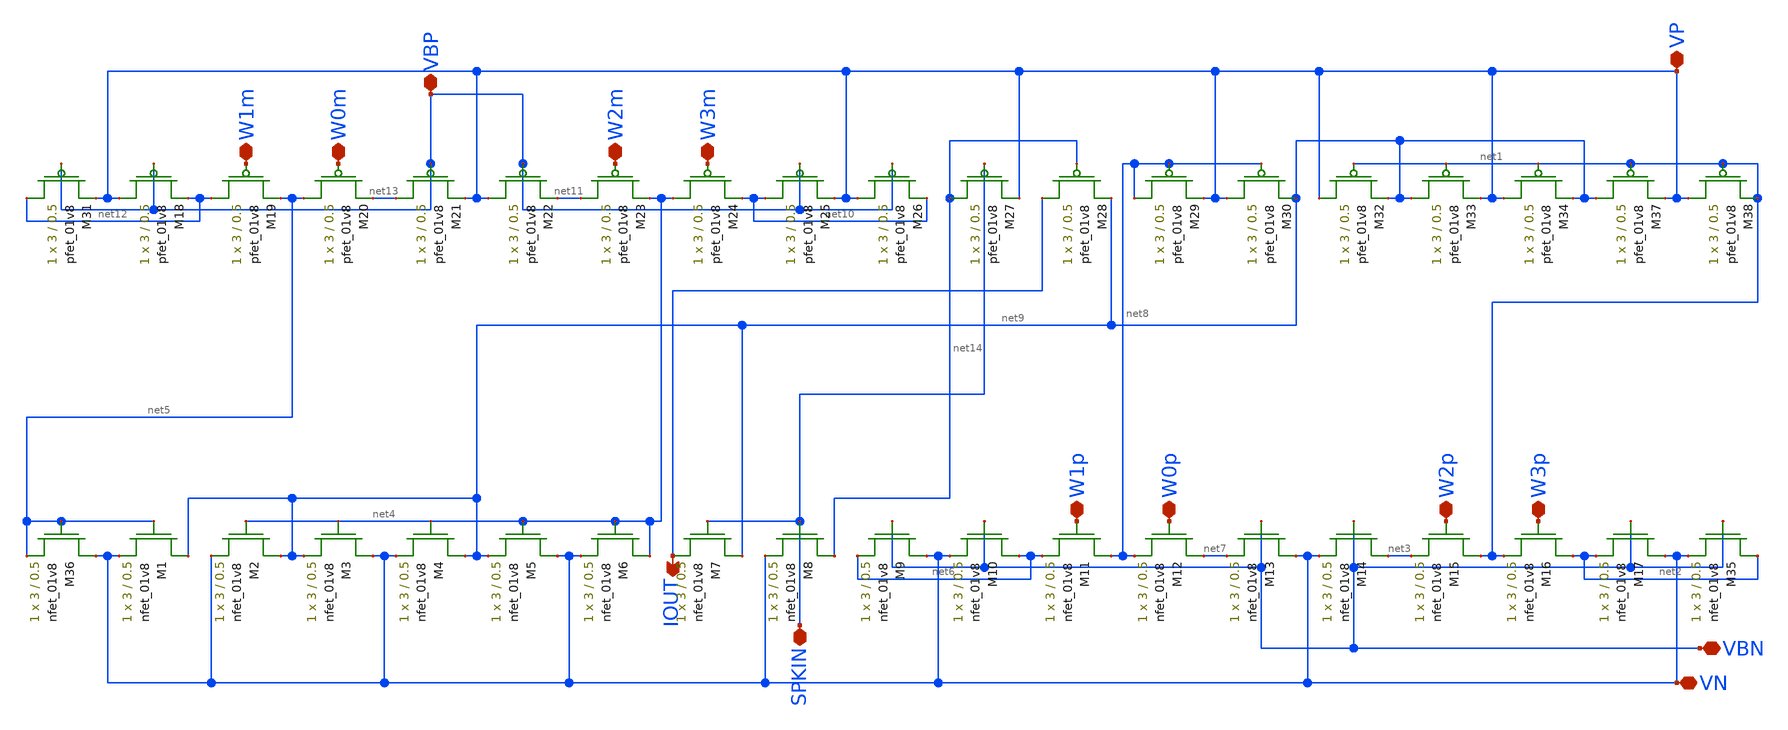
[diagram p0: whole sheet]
** sch_path: schematic/CMCI_synapse_lds.sch
**.subckt CMCI_synapse_lds VBN W3p W2p W0p W1p VBP W3m W2m W0m W1m IOUT SPKIN VP VN
*.iopin VBN
*.iopin W3p
*.iopin W2p
*.iopin W0p
*.iopin W1p
*.iopin VBP
*.iopin W3m
*.iopin W2m
*.iopin W0m
*.iopin W1m
*.opin IOUT
*.iopin SPKIN
*.iopin VP
*.iopin VN
XM36 VN net5 net5 VN sky130_fd_pr__nfet_01v8 L=0.5 W=3 nf=1 ad='int((nf+1)/2) * W/nf * 0.29' as='int((nf+2)/2) * W/nf * 0.29'
+ pd='2*int((nf+1)/2) * (W/nf + 0.29)' ps='2*int((nf+2)/2) * (W/nf + 0.29)' nrd='0.29 / W' nrs='0.29 / W'
+ sa=0 sb=0 sd=0 mult=1 m=1
XM31 net12 VBP VP VP sky130_fd_pr__pfet_01v8 L=0.5 W=3 nf=1 ad='int((nf+1)/2) * W/nf * 0.29' as='int((nf+2)/2) * W/nf * 0.29'
+ pd='2*int((nf+1)/2) * (W/nf + 0.29)' ps='2*int((nf+2)/2) * (W/nf + 0.29)' nrd='0.29 / W' nrs='0.29 / W'
+ sa=0 sb=0 sd=0 mult=1 m=1
XM18 VP VBP net12 VP sky130_fd_pr__pfet_01v8 L=0.5 W=3 nf=1 ad='int((nf+1)/2) * W/nf * 0.29' as='int((nf+2)/2) * W/nf * 0.29'
+ pd='2*int((nf+1)/2) * (W/nf + 0.29)' ps='2*int((nf+2)/2) * (W/nf + 0.29)' nrd='0.29 / W' nrs='0.29 / W'
+ sa=0 sb=0 sd=0 mult=1 m=1
XM19 net12 W1m net5 VP sky130_fd_pr__pfet_01v8 L=0.5 W=3 nf=1 ad='int((nf+1)/2) * W/nf * 0.29' as='int((nf+2)/2) * W/nf * 0.29'
+ pd='2*int((nf+1)/2) * (W/nf + 0.29)' ps='2*int((nf+2)/2) * (W/nf + 0.29)' nrd='0.29 / W' nrs='0.29 / W'
+ sa=0 sb=0 sd=0 mult=1 m=1
XM20 net5 W0m net13 VP sky130_fd_pr__pfet_01v8 L=0.5 W=3 nf=1 ad='int((nf+1)/2) * W/nf * 0.29' as='int((nf+2)/2) * W/nf * 0.29'
+ pd='2*int((nf+1)/2) * (W/nf + 0.29)' ps='2*int((nf+2)/2) * (W/nf + 0.29)' nrd='0.29 / W' nrs='0.29 / W'
+ sa=0 sb=0 sd=0 mult=1 m=1
XM21 net13 VBP VP VP sky130_fd_pr__pfet_01v8 L=0.5 W=3 nf=1 ad='int((nf+1)/2) * W/nf * 0.29' as='int((nf+2)/2) * W/nf * 0.29'
+ pd='2*int((nf+1)/2) * (W/nf + 0.29)' ps='2*int((nf+2)/2) * (W/nf + 0.29)' nrd='0.29 / W' nrs='0.29 / W'
+ sa=0 sb=0 sd=0 mult=1 m=1
XM22 VP VBP net11 VP sky130_fd_pr__pfet_01v8 L=0.5 W=3 nf=1 ad='int((nf+1)/2) * W/nf * 0.29' as='int((nf+2)/2) * W/nf * 0.29'
+ pd='2*int((nf+1)/2) * (W/nf + 0.29)' ps='2*int((nf+2)/2) * (W/nf + 0.29)' nrd='0.29 / W' nrs='0.29 / W'
+ sa=0 sb=0 sd=0 mult=1 m=1
XM23 net11 W2m net4 VP sky130_fd_pr__pfet_01v8 L=0.5 W=3 nf=1 ad='int((nf+1)/2) * W/nf * 0.29' as='int((nf+2)/2) * W/nf * 0.29'
+ pd='2*int((nf+1)/2) * (W/nf + 0.29)' ps='2*int((nf+2)/2) * (W/nf + 0.29)' nrd='0.29 / W' nrs='0.29 / W'
+ sa=0 sb=0 sd=0 mult=1 m=1
XM24 net4 W3m net10 VP sky130_fd_pr__pfet_01v8 L=0.5 W=3 nf=1 ad='int((nf+1)/2) * W/nf * 0.29' as='int((nf+2)/2) * W/nf * 0.29'
+ pd='2*int((nf+1)/2) * (W/nf + 0.29)' ps='2*int((nf+2)/2) * (W/nf + 0.29)' nrd='0.29 / W' nrs='0.29 / W'
+ sa=0 sb=0 sd=0 mult=1 m=1
XM25 net10 VBP VP VP sky130_fd_pr__pfet_01v8 L=0.5 W=3 nf=1 ad='int((nf+1)/2) * W/nf * 0.29' as='int((nf+2)/2) * W/nf * 0.29'
+ pd='2*int((nf+1)/2) * (W/nf + 0.29)' ps='2*int((nf+2)/2) * (W/nf + 0.29)' nrd='0.29 / W' nrs='0.29 / W'
+ sa=0 sb=0 sd=0 mult=1 m=1
XM26 VP VBP net10 VP sky130_fd_pr__pfet_01v8 L=0.5 W=3 nf=1 ad='int((nf+1)/2) * W/nf * 0.29' as='int((nf+2)/2) * W/nf * 0.29'
+ pd='2*int((nf+1)/2) * (W/nf + 0.29)' ps='2*int((nf+2)/2) * (W/nf + 0.29)' nrd='0.29 / W' nrs='0.29 / W'
+ sa=0 sb=0 sd=0 mult=1 m=1
XM27 net14 SPKIN VP VP sky130_fd_pr__pfet_01v8 L=0.5 W=3 nf=1 ad='int((nf+1)/2) * W/nf * 0.29' as='int((nf+2)/2) * W/nf * 0.29'
+ pd='2*int((nf+1)/2) * (W/nf + 0.29)' ps='2*int((nf+2)/2) * (W/nf + 0.29)' nrd='0.29 / W' nrs='0.29 / W'
+ sa=0 sb=0 sd=0 mult=1 m=1
XM28 IOUT net14 net9 VP sky130_fd_pr__pfet_01v8 L=0.5 W=3 nf=1 ad='int((nf+1)/2) * W/nf * 0.29' as='int((nf+2)/2) * W/nf * 0.29'
+ pd='2*int((nf+1)/2) * (W/nf + 0.29)' ps='2*int((nf+2)/2) * (W/nf + 0.29)' nrd='0.29 / W' nrs='0.29 / W'
+ sa=0 sb=0 sd=0 mult=1 m=1
XM29 net8 net8 VP VP sky130_fd_pr__pfet_01v8 L=0.5 W=3 nf=1 ad='int((nf+1)/2) * W/nf * 0.29' as='int((nf+2)/2) * W/nf * 0.29'
+ pd='2*int((nf+1)/2) * (W/nf + 0.29)' ps='2*int((nf+2)/2) * (W/nf + 0.29)' nrd='0.29 / W' nrs='0.29 / W'
+ sa=0 sb=0 sd=0 mult=1 m=1
XM30 VP net8 net9 VP sky130_fd_pr__pfet_01v8 L=0.5 W=3 nf=1 ad='int((nf+1)/2) * W/nf * 0.29' as='int((nf+2)/2) * W/nf * 0.29'
+ pd='2*int((nf+1)/2) * (W/nf + 0.29)' ps='2*int((nf+2)/2) * (W/nf + 0.29)' nrd='0.29 / W' nrs='0.29 / W'
+ sa=0 sb=0 sd=0 mult=1 m=1
XM32 VP net1 net9 VP sky130_fd_pr__pfet_01v8 L=0.5 W=3 nf=1 ad='int((nf+1)/2) * W/nf * 0.29' as='int((nf+2)/2) * W/nf * 0.29'
+ pd='2*int((nf+1)/2) * (W/nf + 0.29)' ps='2*int((nf+2)/2) * (W/nf + 0.29)' nrd='0.29 / W' nrs='0.29 / W'
+ sa=0 sb=0 sd=0 mult=1 m=1
XM33 net9 net1 VP VP sky130_fd_pr__pfet_01v8 L=0.5 W=3 nf=1 ad='int((nf+1)/2) * W/nf * 0.29' as='int((nf+2)/2) * W/nf * 0.29'
+ pd='2*int((nf+1)/2) * (W/nf + 0.29)' ps='2*int((nf+2)/2) * (W/nf + 0.29)' nrd='0.29 / W' nrs='0.29 / W'
+ sa=0 sb=0 sd=0 mult=1 m=1
XM34 VP net1 net9 VP sky130_fd_pr__pfet_01v8 L=0.5 W=3 nf=1 ad='int((nf+1)/2) * W/nf * 0.29' as='int((nf+2)/2) * W/nf * 0.29'
+ pd='2*int((nf+1)/2) * (W/nf + 0.29)' ps='2*int((nf+2)/2) * (W/nf + 0.29)' nrd='0.29 / W' nrs='0.29 / W'
+ sa=0 sb=0 sd=0 mult=1 m=1
XM37 net9 net1 VP VP sky130_fd_pr__pfet_01v8 L=0.5 W=3 nf=1 ad='int((nf+1)/2) * W/nf * 0.29' as='int((nf+2)/2) * W/nf * 0.29'
+ pd='2*int((nf+1)/2) * (W/nf + 0.29)' ps='2*int((nf+2)/2) * (W/nf + 0.29)' nrd='0.29 / W' nrs='0.29 / W'
+ sa=0 sb=0 sd=0 mult=1 m=1
XM38 VP net1 net1 VP sky130_fd_pr__pfet_01v8 L=0.5 W=3 nf=1 ad='int((nf+1)/2) * W/nf * 0.29' as='int((nf+2)/2) * W/nf * 0.29'
+ pd='2*int((nf+1)/2) * (W/nf + 0.29)' ps='2*int((nf+2)/2) * (W/nf + 0.29)' nrd='0.29 / W' nrs='0.29 / W'
+ sa=0 sb=0 sd=0 mult=1 m=1
XM1 net9 net5 VN VN sky130_fd_pr__nfet_01v8 L=0.5 W=3 nf=1 ad='int((nf+1)/2) * W/nf * 0.29' as='int((nf+2)/2) * W/nf * 0.29'
+ pd='2*int((nf+1)/2) * (W/nf + 0.29)' ps='2*int((nf+2)/2) * (W/nf + 0.29)' nrd='0.29 / W' nrs='0.29 / W'
+ sa=0 sb=0 sd=0 mult=1 m=1
XM2 net9 net4 VN VN sky130_fd_pr__nfet_01v8 L=0.5 W=3 nf=1 ad='int((nf+1)/2) * W/nf * 0.29' as='int((nf+2)/2) * W/nf * 0.29'
+ pd='2*int((nf+1)/2) * (W/nf + 0.29)' ps='2*int((nf+2)/2) * (W/nf + 0.29)' nrd='0.29 / W' nrs='0.29 / W'
+ sa=0 sb=0 sd=0 mult=1 m=1
XM3 VN net4 net9 VN sky130_fd_pr__nfet_01v8 L=0.5 W=3 nf=1 ad='int((nf+1)/2) * W/nf * 0.29' as='int((nf+2)/2) * W/nf * 0.29'
+ pd='2*int((nf+1)/2) * (W/nf + 0.29)' ps='2*int((nf+2)/2) * (W/nf + 0.29)' nrd='0.29 / W' nrs='0.29 / W'
+ sa=0 sb=0 sd=0 mult=1 m=1
XM4 net9 net4 VN VN sky130_fd_pr__nfet_01v8 L=0.5 W=3 nf=1 ad='int((nf+1)/2) * W/nf * 0.29' as='int((nf+2)/2) * W/nf * 0.29'
+ pd='2*int((nf+1)/2) * (W/nf + 0.29)' ps='2*int((nf+2)/2) * (W/nf + 0.29)' nrd='0.29 / W' nrs='0.29 / W'
+ sa=0 sb=0 sd=0 mult=1 m=1
XM5 VN net4 net9 VN sky130_fd_pr__nfet_01v8 L=0.5 W=3 nf=1 ad='int((nf+1)/2) * W/nf * 0.29' as='int((nf+2)/2) * W/nf * 0.29'
+ pd='2*int((nf+1)/2) * (W/nf + 0.29)' ps='2*int((nf+2)/2) * (W/nf + 0.29)' nrd='0.29 / W' nrs='0.29 / W'
+ sa=0 sb=0 sd=0 mult=1 m=1
XM6 net4 net4 VN VN sky130_fd_pr__nfet_01v8 L=0.5 W=3 nf=1 ad='int((nf+1)/2) * W/nf * 0.29' as='int((nf+2)/2) * W/nf * 0.29'
+ pd='2*int((nf+1)/2) * (W/nf + 0.29)' ps='2*int((nf+2)/2) * (W/nf + 0.29)' nrd='0.29 / W' nrs='0.29 / W'
+ sa=0 sb=0 sd=0 mult=1 m=1
XM7 net9 SPKIN IOUT VN sky130_fd_pr__nfet_01v8 L=0.5 W=3 nf=1 ad='int((nf+1)/2) * W/nf * 0.29' as='int((nf+2)/2) * W/nf * 0.29'
+ pd='2*int((nf+1)/2) * (W/nf + 0.29)' ps='2*int((nf+2)/2) * (W/nf + 0.29)' nrd='0.29 / W' nrs='0.29 / W'
+ sa=0 sb=0 sd=0 mult=1 m=1
XM8 net14 SPKIN VN VN sky130_fd_pr__nfet_01v8 L=0.5 W=3 nf=1 ad='int((nf+1)/2) * W/nf * 0.29' as='int((nf+2)/2) * W/nf * 0.29'
+ pd='2*int((nf+1)/2) * (W/nf + 0.29)' ps='2*int((nf+2)/2) * (W/nf + 0.29)' nrd='0.29 / W' nrs='0.29 / W'
+ sa=0 sb=0 sd=0 mult=1 m=1
XM9 VN VBN net6 VN sky130_fd_pr__nfet_01v8 L=0.5 W=3 nf=1 ad='int((nf+1)/2) * W/nf * 0.29' as='int((nf+2)/2) * W/nf * 0.29'
+ pd='2*int((nf+1)/2) * (W/nf + 0.29)' ps='2*int((nf+2)/2) * (W/nf + 0.29)' nrd='0.29 / W' nrs='0.29 / W'
+ sa=0 sb=0 sd=0 mult=1 m=1
XM10 net6 VBN VN VN sky130_fd_pr__nfet_01v8 L=0.5 W=3 nf=1 ad='int((nf+1)/2) * W/nf * 0.29' as='int((nf+2)/2) * W/nf * 0.29'
+ pd='2*int((nf+1)/2) * (W/nf + 0.29)' ps='2*int((nf+2)/2) * (W/nf + 0.29)' nrd='0.29 / W' nrs='0.29 / W'
+ sa=0 sb=0 sd=0 mult=1 m=1
XM11 net8 W1p net6 VN sky130_fd_pr__nfet_01v8 L=0.5 W=3 nf=1 ad='int((nf+1)/2) * W/nf * 0.29' as='int((nf+2)/2) * W/nf * 0.29'
+ pd='2*int((nf+1)/2) * (W/nf + 0.29)' ps='2*int((nf+2)/2) * (W/nf + 0.29)' nrd='0.29 / W' nrs='0.29 / W'
+ sa=0 sb=0 sd=0 mult=1 m=1
XM12 net7 W0p net8 VN sky130_fd_pr__nfet_01v8 L=0.5 W=3 nf=1 ad='int((nf+1)/2) * W/nf * 0.29' as='int((nf+2)/2) * W/nf * 0.29'
+ pd='2*int((nf+1)/2) * (W/nf + 0.29)' ps='2*int((nf+2)/2) * (W/nf + 0.29)' nrd='0.29 / W' nrs='0.29 / W'
+ sa=0 sb=0 sd=0 mult=1 m=1
XM13 VN VBN net7 VN sky130_fd_pr__nfet_01v8 L=0.5 W=3 nf=1 ad='int((nf+1)/2) * W/nf * 0.29' as='int((nf+2)/2) * W/nf * 0.29'
+ pd='2*int((nf+1)/2) * (W/nf + 0.29)' ps='2*int((nf+2)/2) * (W/nf + 0.29)' nrd='0.29 / W' nrs='0.29 / W'
+ sa=0 sb=0 sd=0 mult=1 m=1
XM14 net3 VBN VN VN sky130_fd_pr__nfet_01v8 L=0.5 W=3 nf=1 ad='int((nf+1)/2) * W/nf * 0.29' as='int((nf+2)/2) * W/nf * 0.29'
+ pd='2*int((nf+1)/2) * (W/nf + 0.29)' ps='2*int((nf+2)/2) * (W/nf + 0.29)' nrd='0.29 / W' nrs='0.29 / W'
+ sa=0 sb=0 sd=0 mult=1 m=1
XM15 net1 W2p net3 VN sky130_fd_pr__nfet_01v8 L=0.5 W=3 nf=1 ad='int((nf+1)/2) * W/nf * 0.29' as='int((nf+2)/2) * W/nf * 0.29'
+ pd='2*int((nf+1)/2) * (W/nf + 0.29)' ps='2*int((nf+2)/2) * (W/nf + 0.29)' nrd='0.29 / W' nrs='0.29 / W'
+ sa=0 sb=0 sd=0 mult=1 m=1
XM16 net2 W3p net1 VN sky130_fd_pr__nfet_01v8 L=0.5 W=3 nf=1 ad='int((nf+1)/2) * W/nf * 0.29' as='int((nf+2)/2) * W/nf * 0.29'
+ pd='2*int((nf+1)/2) * (W/nf + 0.29)' ps='2*int((nf+2)/2) * (W/nf + 0.29)' nrd='0.29 / W' nrs='0.29 / W'
+ sa=0 sb=0 sd=0 mult=1 m=1
XM17 VN VBN net2 VN sky130_fd_pr__nfet_01v8 L=0.5 W=3 nf=1 ad='int((nf+1)/2) * W/nf * 0.29' as='int((nf+2)/2) * W/nf * 0.29'
+ pd='2*int((nf+1)/2) * (W/nf + 0.29)' ps='2*int((nf+2)/2) * (W/nf + 0.29)' nrd='0.29 / W' nrs='0.29 / W'
+ sa=0 sb=0 sd=0 mult=1 m=1
XM35 net2 VBN VN VN sky130_fd_pr__nfet_01v8 L=0.5 W=3 nf=1 ad='int((nf+1)/2) * W/nf * 0.29' as='int((nf+2)/2) * W/nf * 0.29'
+ pd='2*int((nf+1)/2) * (W/nf + 0.29)' ps='2*int((nf+2)/2) * (W/nf + 0.29)' nrd='0.29 / W' nrs='0.29 / W'
+ sa=0 sb=0 sd=0 mult=1 m=1
**.ends
.end
